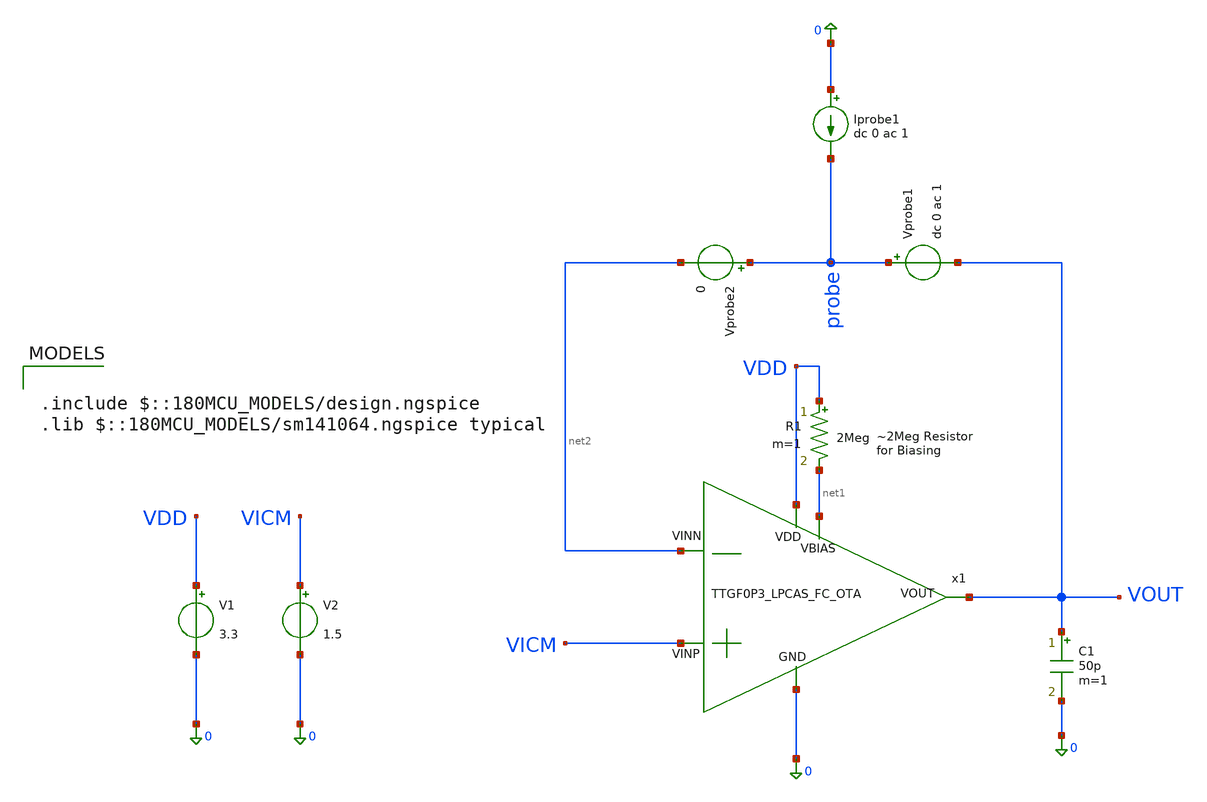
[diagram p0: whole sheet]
** sch_path: SCH/XSCHEM_SCH/tb_TTGF0P3_LPCAS_FC_OTA_STB.sch
**.subckt tb_TTGF0P3_LPCAS_FC_OTA_STB
x1 VDD net1 VOUT VICM net2 0 TTGF0P3_LPCAS_FC_OTA
V1 VDD 0 3.3
V2 VICM 0 1.5
R1 VDD net1 2Meg m=1
C1 VOUT 0 50p m=1
Vprobe1 probe VOUT dc 0 ac 1
Vprobe2 probe net2 0
Iprobe1 0 probe dc 0 ac 1
**** begin user architecture code

.include $::180MCU_MODELS/design.ngspice
.lib $::180MCU_MODELS/sm141064.ngspice typical



.options savecurrents
.control
 save all
 let runs=2
 let run=0

 alter @Vprobe1[acmag]=1
 alter @iprobe1[acmag]=0

 dowhile run < runs
 set run =”$&run”
 ac dec 20 1 1e8
 write tb_TTGF0P3_LPCAS_FC_OTA_{$run}.raw
 all
 alter @Vprobe1[acmag]=0
 alter @iprobe1[acmag]=1
 let run = run + 1
 end

 let ip22 = ac2.i(Vprobe2)
 let vprb1 = ac1.probe
 let mb = 1/(vprb1+ip22)-1
 let phase_mb = 180/PI*vp(mb)
 plot vdb(mb)
 plot phase_mb
 plot vdb(mb) phase_mb
 echo -------------------------------
 echo -------------------------------
 meas ac peak MAX vmag(mb) FROM=2 TO=1.5GHZ
 let f3db = peak/sqrt(2)
 meas ac f1 WHEN vmag(mb)=f3db RISE=1
 meas ac BW WHEN vmag(mb)=f3db FALL=1
 let GBW = peak*BW
 meas ac pm_deg find phase_mb when vdb(mb)=0
 meas ac dominant_pole_f when vdb(mb)=0
 meas ac loop_gain find vdb(mb) at=0.01
 print GBW
 op
 **show m : gm : gmbs : gds : vds : vdsat : vgs : vth : id
.endc

**** end user architecture code
**.ends

* expanding   symbol:  /home/nithin/eda/ttgf0p3/TTGF0P3_LPCAS_FC_OTA.sym # of pins=6
** sym_path: SCH/TTGF0P3_LPCAS_FC_OTA.sym
** sch_path: SCH/TTGF0P3_LPCAS_FC_OTA.sch
.subckt TTGF0P3_LPCAS_FC_OTA VDD VBIAS VOUT VINP VINN GND
*.opin VOUT
*.ipin VINP
*.ipin VINN
*.ipin VDD
*.ipin VBIAS
*.ipin GND
XM1 net11 VBIASCN net1 GND nfet_03v3 L=1u W=4u nf=1 ad='int((nf+1)/2) * W/nf * 0.18u' as='int((nf+2)/2) * W/nf * 0.18u'
+ pd='2*int((nf+1)/2) * (W/nf + 0.18u)' ps='2*int((nf+2)/2) * (W/nf + 0.18u)' nrd='0.18u / W' nrs='0.18u / W'
+ sa=0 sb=0 sd=0 m=1
XM2 VOUT VBIASCN net2 GND nfet_03v3 L=1u W=3u nf=1 ad='int((nf+1)/2) * W/nf * 0.18u' as='int((nf+2)/2) * W/nf * 0.18u'
+ pd='2*int((nf+1)/2) * (W/nf + 0.18u)' ps='2*int((nf+2)/2) * (W/nf + 0.18u)' nrd='0.18u / W' nrs='0.18u / W'
+ sa=0 sb=0 sd=0 m=1
XM5 net12 VBIASCP net4 VDD pfet_03v3 L=0.3u W=3u nf=1 ad='int((nf+1)/2) * W/nf * 0.18u' as='int((nf+2)/2) * W/nf * 0.18u'
+ pd='2*int((nf+1)/2) * (W/nf + 0.18u)' ps='2*int((nf+2)/2) * (W/nf + 0.18u)' nrd='0.18u / W' nrs='0.18u / W'
+ sa=0 sb=0 sd=0 m=1
XM6 net5 VBIASCP net3 VDD pfet_03v3 L=0.3u W=3u nf=1 ad='int((nf+1)/2) * W/nf * 0.18u' as='int((nf+2)/2) * W/nf * 0.18u'
+ pd='2*int((nf+1)/2) * (W/nf + 0.18u)' ps='2*int((nf+2)/2) * (W/nf + 0.18u)' nrd='0.18u / W' nrs='0.18u / W'
+ sa=0 sb=0 sd=0 m=1
XM7 net4 net5 net13 VDD pfet_03v3 L=1u W=8u nf=1 ad='int((nf+1)/2) * W/nf * 0.18u' as='int((nf+2)/2) * W/nf * 0.18u'
+ pd='2*int((nf+1)/2) * (W/nf + 0.18u)' ps='2*int((nf+2)/2) * (W/nf + 0.18u)' nrd='0.18u / W' nrs='0.18u / W'
+ sa=0 sb=0 sd=0 m=6
XM8 net3 net5 net14 VDD pfet_03v3 L=1u W=8u nf=1 ad='int((nf+1)/2) * W/nf * 0.18u' as='int((nf+2)/2) * W/nf * 0.18u'
+ pd='2*int((nf+1)/2) * (W/nf + 0.18u)' ps='2*int((nf+2)/2) * (W/nf + 0.18u)' nrd='0.18u / W' nrs='0.18u / W'
+ sa=0 sb=0 sd=0 m=6
XM9 VBIAS VBIAS GND GND nfet_03v3 L=3u W=2u nf=1 ad='int((nf+1)/2) * W/nf * 0.18u' as='int((nf+2)/2) * W/nf * 0.18u'
+ pd='2*int((nf+1)/2) * (W/nf + 0.18u)' ps='2*int((nf+2)/2) * (W/nf + 0.18u)' nrd='0.18u / W' nrs='0.18u / W'
+ sa=0 sb=0 sd=0 m=1
XM10 net9 VBIAS GND GND nfet_03v3 L=3u W=2u nf=1 ad='int((nf+1)/2) * W/nf * 0.18u' as='int((nf+2)/2) * W/nf * 0.18u'
+ pd='2*int((nf+1)/2) * (W/nf + 0.18u)' ps='2*int((nf+2)/2) * (W/nf + 0.18u)' nrd='0.18u / W' nrs='0.18u / W'
+ sa=0 sb=0 sd=0 m=5
XM3 net1 VBIAS GND GND nfet_03v3 L=3u W=2u nf=1 ad='int((nf+1)/2) * W/nf * 0.18u' as='int((nf+2)/2) * W/nf * 0.18u'
+ pd='2*int((nf+1)/2) * (W/nf + 0.18u)' ps='2*int((nf+2)/2) * (W/nf + 0.18u)' nrd='0.18u / W' nrs='0.18u / W'
+ sa=0 sb=0 sd=0 m=1
XM4 net2 VBIAS GND GND nfet_03v3 L=3u W=2u nf=1 ad='int((nf+1)/2) * W/nf * 0.18u' as='int((nf+2)/2) * W/nf * 0.18u'
+ pd='2*int((nf+1)/2) * (W/nf + 0.18u)' ps='2*int((nf+2)/2) * (W/nf + 0.18u)' nrd='0.18u / W' nrs='0.18u / W'
+ sa=0 sb=0 sd=0 m=1
XM14 net10 VBIAS GND GND nfet_03v3 L=3u W=2u nf=1 ad='int((nf+1)/2) * W/nf * 0.18u' as='int((nf+2)/2) * W/nf * 0.18u'
+ pd='2*int((nf+1)/2) * (W/nf + 0.18u)' ps='2*int((nf+2)/2) * (W/nf + 0.18u)' nrd='0.18u / W' nrs='0.18u / W'
+ sa=0 sb=0 sd=0 m=1
XM15 net15 VBIASCP VDD VDD pfet_03v3 L=0.3u W=0.3u nf=1 ad='int((nf+1)/2) * W/nf * 0.18u' as='int((nf+2)/2) * W/nf * 0.18u'
+ pd='2*int((nf+1)/2) * (W/nf + 0.18u)' ps='2*int((nf+2)/2) * (W/nf + 0.18u)' nrd='0.18u / W' nrs='0.18u / W'
+ sa=0 sb=0 sd=0 m=1
Vmeas net3 net7 0
.save i(vmeas)
Vmeas1 net4 net8 0
.save i(vmeas1)
Vmeas2 net6 net9 0
.save i(vmeas2)
Vmeas3 VBIASCP net10 0
.save i(vmeas3)
Vmeas4 net5 net11 0
.save i(vmeas4)
Vmeas5 net12 VOUT 0
.save i(vmeas5)
XM16 net7 VINP net6 GND nfet_03v3 L=1u W=8.5u nf=1 ad='int((nf+1)/2) * W/nf * 0.18u' as='int((nf+2)/2) * W/nf * 0.18u'
+ pd='2*int((nf+1)/2) * (W/nf + 0.18u)' ps='2*int((nf+2)/2) * (W/nf + 0.18u)' nrd='0.18u / W' nrs='0.18u / W'
+ sa=0 sb=0 sd=0 m=4
XM11 net8 VINN net6 GND nfet_03v3 L=1u W=8.5u nf=1 ad='int((nf+1)/2) * W/nf * 0.18u' as='int((nf+2)/2) * W/nf * 0.18u'
+ pd='2*int((nf+1)/2) * (W/nf + 0.18u)' ps='2*int((nf+2)/2) * (W/nf + 0.18u)' nrd='0.18u / W' nrs='0.18u / W'
+ sa=0 sb=0 sd=0 m=4
Vmeas6 VDD net14 0
.save i(vmeas6)
Vmeas7 VDD net13 0
.save i(vmeas7)
C1 VOUT GND 100p m=1
XM12 VBIASCP VBIASCP net15 VDD pfet_03v3 L=0.3u W=0.3u nf=1 ad='int((nf+1)/2) * W/nf * 0.18u' as='int((nf+2)/2) * W/nf * 0.18u'
+ pd='2*int((nf+1)/2) * (W/nf + 0.18u)' ps='2*int((nf+2)/2) * (W/nf + 0.18u)' nrd='0.18u / W' nrs='0.18u / W'
+ sa=0 sb=0 sd=0 m=1
XM17 net16 VBIASCP VDD VDD pfet_03v3 L=0.3u W=0.3u nf=1 ad='int((nf+1)/2) * W/nf * 0.18u' as='int((nf+2)/2) * W/nf * 0.18u'
+ pd='2*int((nf+1)/2) * (W/nf + 0.18u)' ps='2*int((nf+2)/2) * (W/nf + 0.18u)' nrd='0.18u / W' nrs='0.18u / W'
+ sa=0 sb=0 sd=0 m=1
XM18 VBIASCN VBIASCP net16 VDD pfet_03v3 L=0.3u W=0.3u nf=1 ad='int((nf+1)/2) * W/nf * 0.18u' as='int((nf+2)/2) * W/nf * 0.18u'
+ pd='2*int((nf+1)/2) * (W/nf + 0.18u)' ps='2*int((nf+2)/2) * (W/nf + 0.18u)' nrd='0.18u / W' nrs='0.18u / W'
+ sa=0 sb=0 sd=0 m=1
XM19 net17 VBIASCN GND GND nfet_03v3 L=1u W=1u nf=1 ad='int((nf+1)/2) * W/nf * 0.18u' as='int((nf+2)/2) * W/nf * 0.18u'
+ pd='2*int((nf+1)/2) * (W/nf + 0.18u)' ps='2*int((nf+2)/2) * (W/nf + 0.18u)' nrd='0.18u / W' nrs='0.18u / W'
+ sa=0 sb=0 sd=0 m=1
XM20 net18 VBIASCN net17 GND nfet_03v3 L=1u W=1u nf=1 ad='int((nf+1)/2) * W/nf * 0.18u' as='int((nf+2)/2) * W/nf * 0.18u'
+ pd='2*int((nf+1)/2) * (W/nf + 0.18u)' ps='2*int((nf+2)/2) * (W/nf + 0.18u)' nrd='0.18u / W' nrs='0.18u / W'
+ sa=0 sb=0 sd=0 m=1
XM21 VBIASCN VBIASCN net18 GND nfet_03v3 L=1u W=1u nf=1 ad='int((nf+1)/2) * W/nf * 0.18u' as='int((nf+2)/2) * W/nf * 0.18u'
+ pd='2*int((nf+1)/2) * (W/nf + 0.18u)' ps='2*int((nf+2)/2) * (W/nf + 0.18u)' nrd='0.18u / W' nrs='0.18u / W'
+ sa=0 sb=0 sd=0 m=1
.ends

.end
